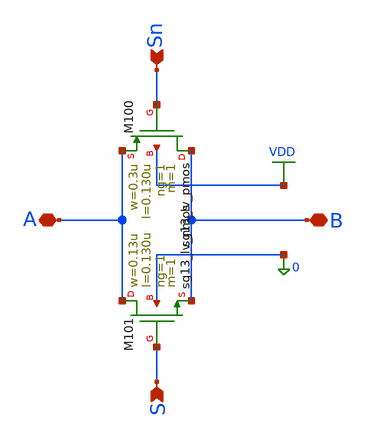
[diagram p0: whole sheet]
** sch_path: Enfoque_A/xschem/Ll.sch
**.subckt Ll B Sn S A
*.iopin B
*.ipin Sn
*.ipin S
*.iopin A
XM101 A S B 0 sg13_lv_nmos w=0.13u l=0.130u ng=1 m=1 mm_ok=1
XM100 B Sn A VDD sg13_lv_pmos w=0.3u l=0.130u ng=1 m=1 mm_ok=1
**.ends
.GLOBAL VDD
.end
